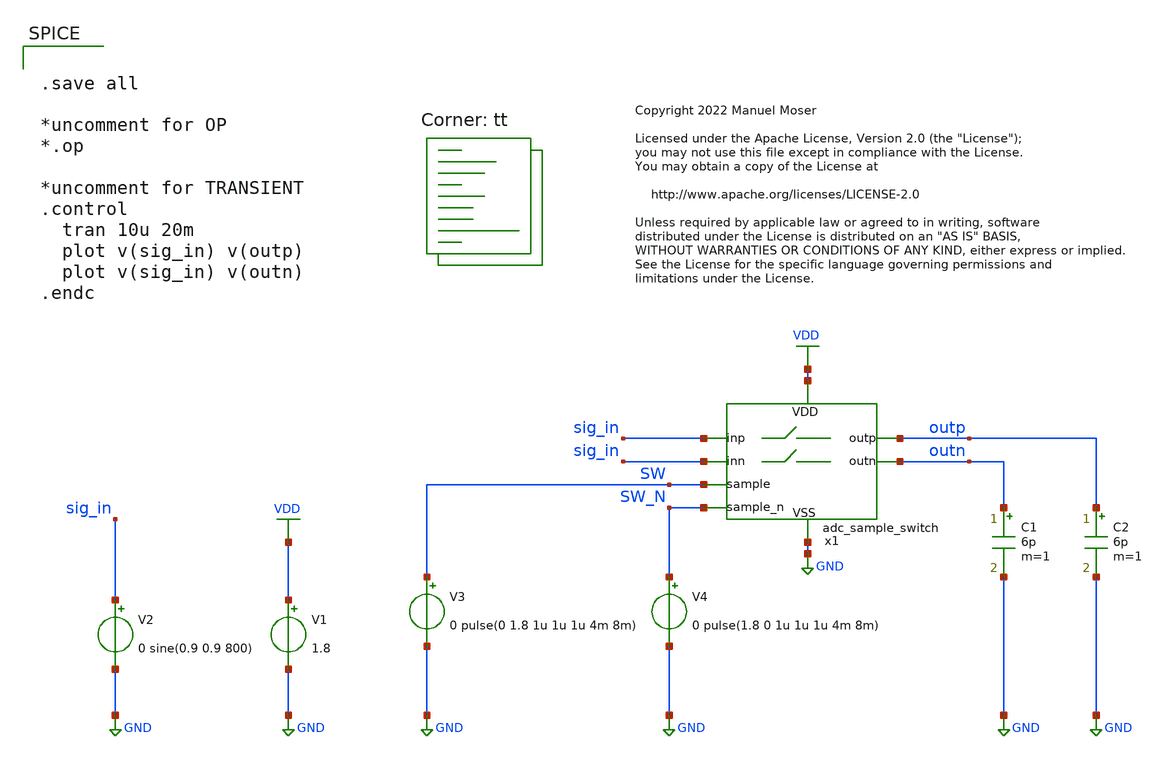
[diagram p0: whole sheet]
** sch_path: xschem/adc_sample_switch/adc_sample_switch_tb.sch
* Copyright 2022 Manuel Moser
* Licensed under the Apache License, Version 2.0 (the "License");
**.subckt adc_sample_switch_tb
V1 VDD GND 1.8
V2 sig_in GND 0 sine(0.9 0.9 800)
V3 SW GND 0 pulse(0 1.8 1u 1u 1u 4m 8m)
V4 SW_N GND 0 pulse(1.8 0 1u 1u 1u 4m 8m)
C1 outn GND 6p m=1
x1 VDD GND SW_N outp sig_in outn sig_in SW adc_sample_switch
C2 outp GND 6p m=1
**** begin user architecture code


.save all

*uncomment for OP
*.op

*uncomment for TRANSIENT
.control
  tran 10u 20m
  plot v(sig_in) v(outp)
  plot v(sig_in) v(outn)
.endc


.lib $::SKYWATER_MODELS/sky130.lib.spice tt
**** end user architecture code
**.ends
.GLOBAL GND
.GLOBAL VDD
.end
